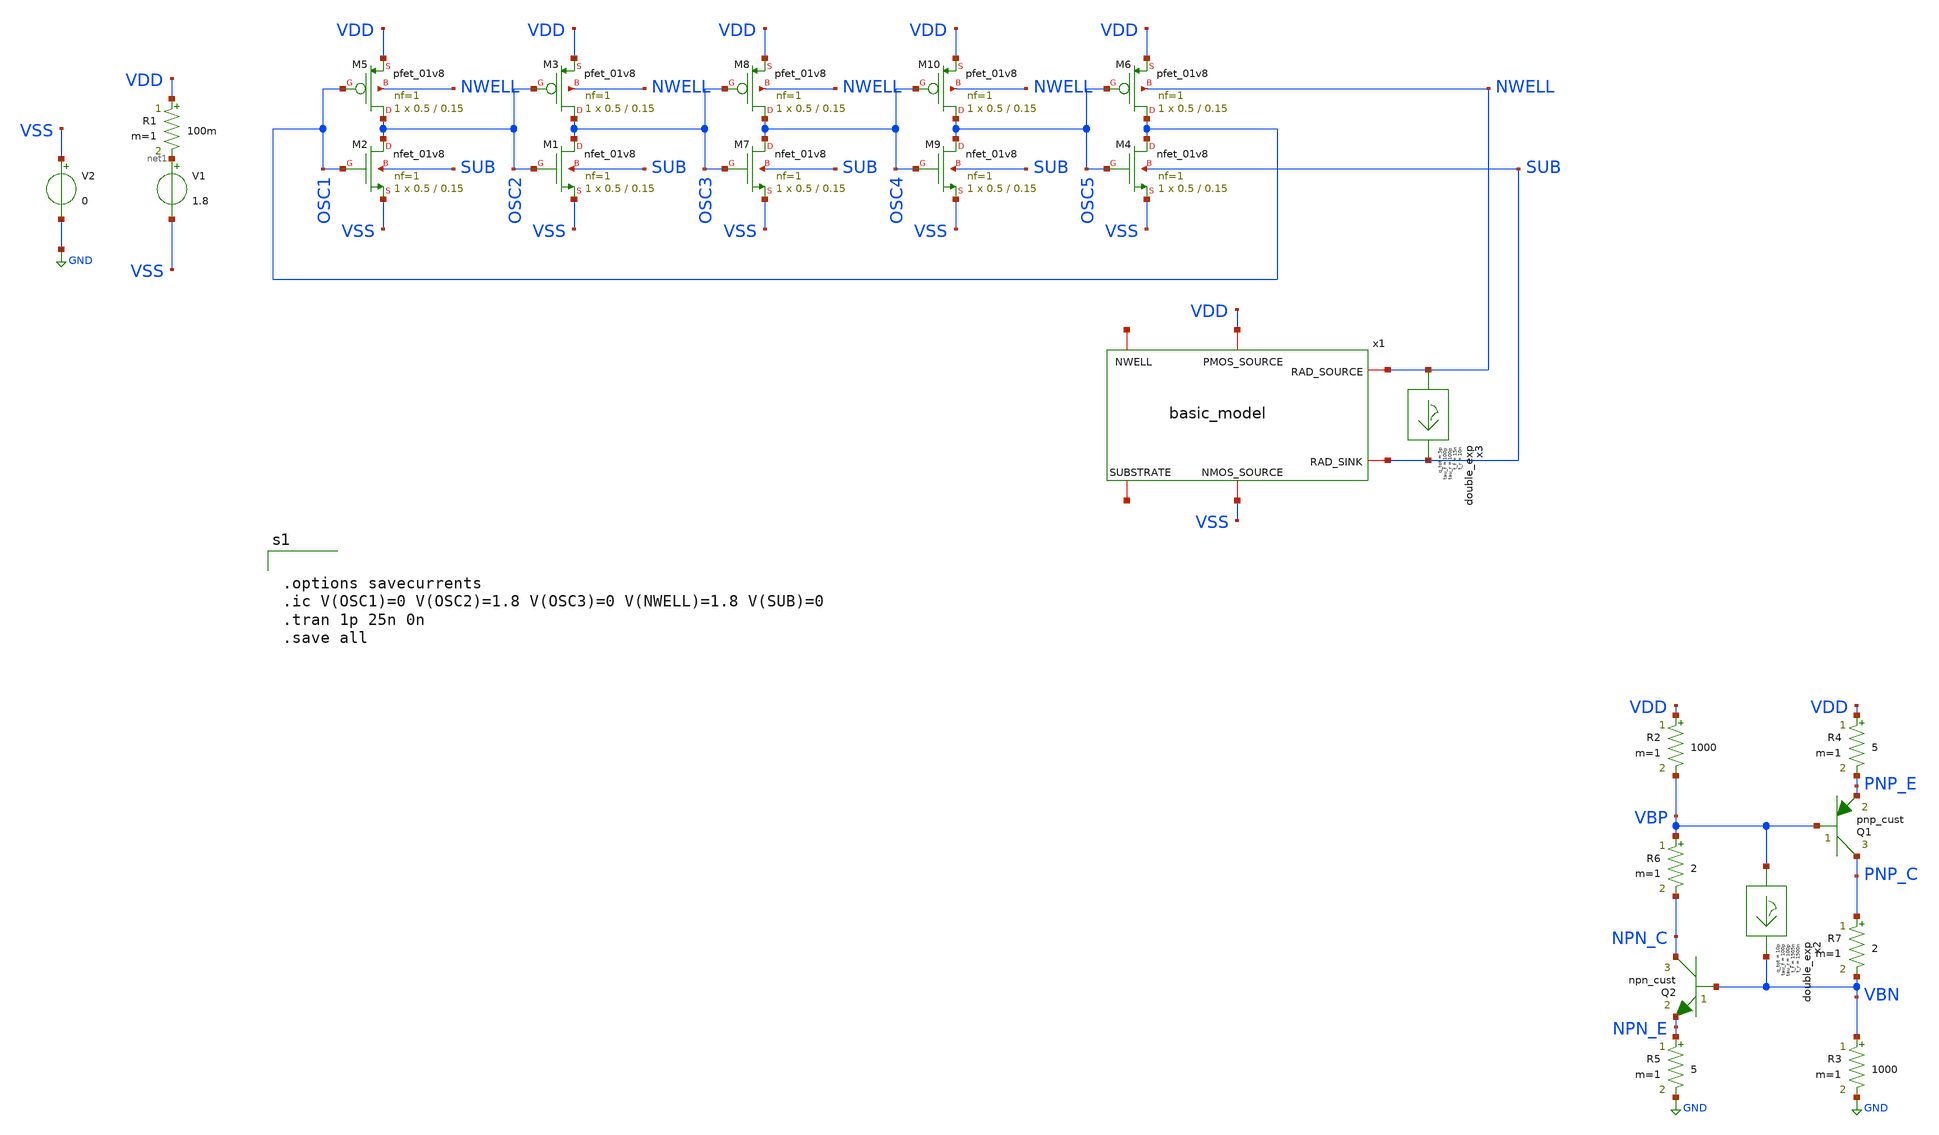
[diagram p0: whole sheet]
** sch_path: latchup/RING_OSC_TEST.sch
**.subckt RING_OSC_TEST
XM2 OSC2 OSC1 VSS SUB sky130_fd_pr__nfet_01v8 L=0.15 W=0.5 nf=1 ad='int((nf+1)/2) * W/nf * 0.29' as='int((nf+2)/2) * W/nf * 0.29'
+ pd='2*int((nf+1)/2) * (W/nf + 0.29)' ps='2*int((nf+2)/2) * (W/nf + 0.29)' nrd='0.29 / W' nrs='0.29 / W'
+ sa=0 sb=0 sd=0 mult=1 m=1
XM5 OSC2 OSC1 VDD NWELL sky130_fd_pr__pfet_01v8 L=0.15 W=0.5 nf=1 ad='int((nf+1)/2) * W/nf * 0.29' as='int((nf+2)/2) * W/nf * 0.29'
+ pd='2*int((nf+1)/2) * (W/nf + 0.29)' ps='2*int((nf+2)/2) * (W/nf + 0.29)' nrd='0.29 / W' nrs='0.29 / W'
+ sa=0 sb=0 sd=0 mult=1 m=1
XM1 OSC3 OSC2 VSS SUB sky130_fd_pr__nfet_01v8 L=0.15 W=0.5 nf=1 ad='int((nf+1)/2) * W/nf * 0.29' as='int((nf+2)/2) * W/nf * 0.29'
+ pd='2*int((nf+1)/2) * (W/nf + 0.29)' ps='2*int((nf+2)/2) * (W/nf + 0.29)' nrd='0.29 / W' nrs='0.29 / W'
+ sa=0 sb=0 sd=0 mult=1 m=1
XM3 OSC3 OSC2 VDD NWELL sky130_fd_pr__pfet_01v8 L=0.15 W=0.5 nf=1 ad='int((nf+1)/2) * W/nf * 0.29' as='int((nf+2)/2) * W/nf * 0.29'
+ pd='2*int((nf+1)/2) * (W/nf + 0.29)' ps='2*int((nf+2)/2) * (W/nf + 0.29)' nrd='0.29 / W' nrs='0.29 / W'
+ sa=0 sb=0 sd=0 mult=1 m=1
XM4 OSC1 OSC5 VSS SUB sky130_fd_pr__nfet_01v8 L=0.15 W=0.5 nf=1 ad='int((nf+1)/2) * W/nf * 0.29' as='int((nf+2)/2) * W/nf * 0.29'
+ pd='2*int((nf+1)/2) * (W/nf + 0.29)' ps='2*int((nf+2)/2) * (W/nf + 0.29)' nrd='0.29 / W' nrs='0.29 / W'
+ sa=0 sb=0 sd=0 mult=1 m=1
XM6 OSC1 OSC5 VDD NWELL sky130_fd_pr__pfet_01v8 L=0.15 W=0.5 nf=1 ad='int((nf+1)/2) * W/nf * 0.29' as='int((nf+2)/2) * W/nf * 0.29'
+ pd='2*int((nf+1)/2) * (W/nf + 0.29)' ps='2*int((nf+2)/2) * (W/nf + 0.29)' nrd='0.29 / W' nrs='0.29 / W'
+ sa=0 sb=0 sd=0 mult=1 m=1
V1 net1 VSS 1.8
V2 VSS GND 0
x3 NWELL SUB double_exp t_r=10n tau_r=100p t_f=15n tau_f=100p q_tot=5p
x1 VDD net2 NWELL SUB VSS net3 basic_model
R1 VDD net1 100m m=1
XM7 OSC4 OSC3 VSS SUB sky130_fd_pr__nfet_01v8 L=0.15 W=0.5 nf=1 ad='int((nf+1)/2) * W/nf * 0.29' as='int((nf+2)/2) * W/nf * 0.29'
+ pd='2*int((nf+1)/2) * (W/nf + 0.29)' ps='2*int((nf+2)/2) * (W/nf + 0.29)' nrd='0.29 / W' nrs='0.29 / W'
+ sa=0 sb=0 sd=0 mult=1 m=1
XM8 OSC4 OSC3 VDD NWELL sky130_fd_pr__pfet_01v8 L=0.15 W=0.5 nf=1 ad='int((nf+1)/2) * W/nf * 0.29' as='int((nf+2)/2) * W/nf * 0.29'
+ pd='2*int((nf+1)/2) * (W/nf + 0.29)' ps='2*int((nf+2)/2) * (W/nf + 0.29)' nrd='0.29 / W' nrs='0.29 / W'
+ sa=0 sb=0 sd=0 mult=1 m=1
XM9 OSC5 OSC4 VSS SUB sky130_fd_pr__nfet_01v8 L=0.15 W=0.5 nf=1 ad='int((nf+1)/2) * W/nf * 0.29' as='int((nf+2)/2) * W/nf * 0.29'
+ pd='2*int((nf+1)/2) * (W/nf + 0.29)' ps='2*int((nf+2)/2) * (W/nf + 0.29)' nrd='0.29 / W' nrs='0.29 / W'
+ sa=0 sb=0 sd=0 mult=1 m=1
XM10 OSC5 OSC4 VDD NWELL sky130_fd_pr__pfet_01v8 L=0.15 W=0.5 nf=1 ad='int((nf+1)/2) * W/nf * 0.29' as='int((nf+2)/2) * W/nf * 0.29'
+ pd='2*int((nf+1)/2) * (W/nf + 0.29)' ps='2*int((nf+2)/2) * (W/nf + 0.29)' nrd='0.29 / W' nrs='0.29 / W'
+ sa=0 sb=0 sd=0 mult=1 m=1
Q1 PNP_C VBP PNP_E pnp_cust area=1 m=1
Q2 NPN_C VBN NPN_E npn_cust area=1 m=1
R3 VBN GND 1000 m=1
R4 VDD PNP_E 5 m=1
R2 VDD VBP 1000 m=1
R5 NPN_E GND 5 m=1
R6 VBP NPN_C 2 m=1
R7 PNP_C VBN 2 m=1
x2 VBP VBN double_exp t_r=1500n tau_r=100p t_f=1505n tau_f=100p q_tot=10p
**** begin user architecture code


.options savecurrents
.ic V(OSC1)=0 V(OSC2)=1.8 V(OSC3)=0 V(NWELL)=1.8 V(SUB)=0
.tran 1p 25n 0n
.save all



** opencircuitdesign pdks install
.lib $::SKYWATER_MODELS/sky130.lib.spice tt




.include /usr/local/share/rad_modeling_blocks/rad_modeling_blocks.spice


**** end user architecture code
**.ends

* expanding   symbol:  double_exp.sym # of pins=2
** sym_path: xschem_rad_library/double_exp.sym
** sch_path: xschem_rad_library/double_exp.sch
.subckt double_exp in out  t_r=0 t_f=0 tau_r=0 tau_f=0 q_tot=0
*.opin OUT
*.ipin IN
I1 IN OUT EXP(0 {q_tot / (t_f-t_r+tau_f-tau_r)} {t_r} {tau_r} {t_f} {tau_f})
.ends


* expanding   symbol:  OSCRE/latchup/basic_model.sym # of pins=6
** sym_path: latchup/basic_model.sym
** sch_path: latchup/basic_model.sch
.subckt basic_model PMOS_SOURCE NWELL RAD_SOURCE RAD_SINK NMOS_SOURCE SUBSTRATE   IS_N=1e-18
+  BF_N=100  VAF_N=50  IKF_N=0.01  CJE_N=0.2p  CJC_N=0.1p  TF_N=0.2n  TR_N=2n  IS_P=1e-18  BF_P=100  VAF_P=50
+  IKF_P=0.01  CJE_P=0.3p  CJC_P=0.15p  TF_P=0.3n  TR_P=3n
*.iopin NWELL
*.iopin SUBSTRATE
*.iopin RAD_SOURCE
*.iopin RAD_SINK
*.iopin NMOS_SOURCE
*.iopin PMOS_SOURCE
Q1 RAD_SINK RAD_SOURCE PMOS_SOURCE pnp_cust area=1 m=1
Q2 RAD_SOURCE RAD_SINK NMOS_SOURCE npn_cust area=1 m=1
R3 RAD_SINK SUBSTRATE 1000 m=1
R4 NWELL RAD_SOURCE 1000 m=1
**** begin user architecture code


.model npn_cust npn (IS={IS_N} BF={BF_N} VAF={VAF_N} IKF={IKF_N} CJE={CJE_N} CJC={CJC_N} TF={TF_N} TR={TR_N})
.model pnp_cust pnp (IS={IS_P} BF={BF_P} VAF={VAF_P} IKF={IKF_P} CJE={CJE_P} CJC={CJC_N} TF={TF_N} TR={TR_P})


**** end user architecture code
.ends

.GLOBAL GND
.end
